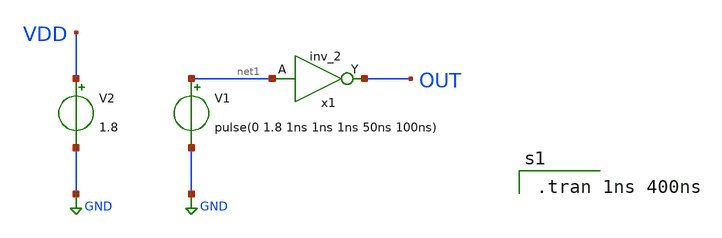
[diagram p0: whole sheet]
** sch_path: opamp_lna/std_cell_tb.sch
**.subckt std_cell_tb
V1 net1 GND pulse(0 1.8 1ns 1ns 1ns 50ns 100ns)
V2 VDD GND 1.8
x1 net1 GND VNB VPB VDD OUT sky130_fd_sc_hd__inv_2
**** begin user architecture code

.tran 1ns 400ns


** opencircuitdesign pdks install
.lib $::SKYWATER_MODELS/sky130.lib.spice tt
.include $::SKYWATER_STDCELLS/sky130_fd_sc_hd.spice

**** end user architecture code
**.ends
.GLOBAL GND
.end
